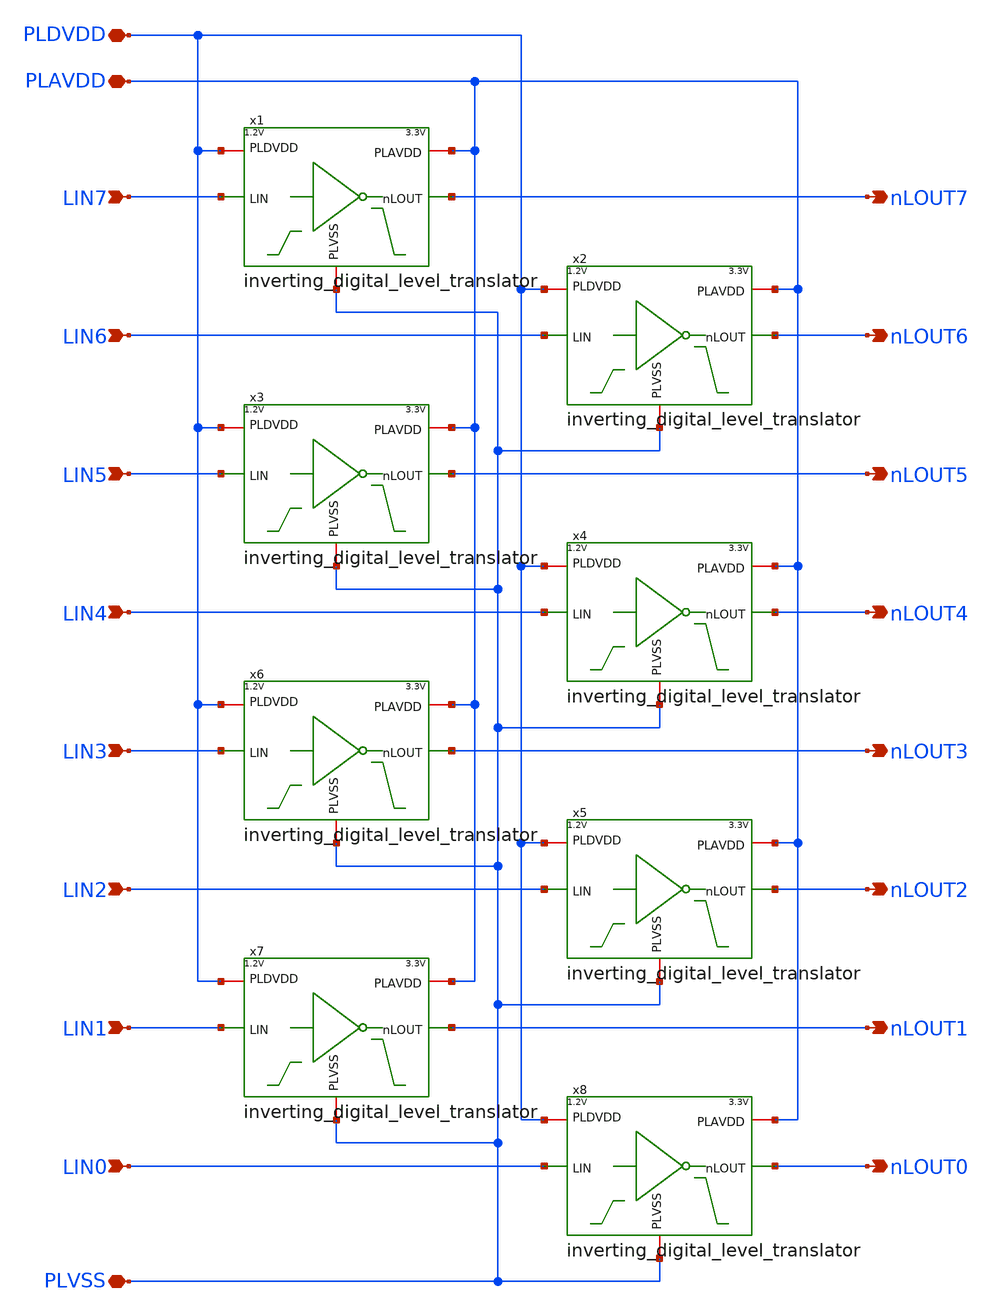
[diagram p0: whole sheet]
** sch_path: xschem/8x_inverting_digital_level_translator.sch
**.subckt 8x_inverting_digital_level_translator LIN7 nLOUT7 PLDVDD PLAVDD PLVSS LIN6 LIN5 LIN4 LIN3
*+ LIN2 LIN1 LIN0 nLOUT6 nLOUT5 nLOUT4 nLOUT3 nLOUT2 nLOUT1 nLOUT0
*.ipin LIN7
*.opin nLOUT7
*.iopin PLDVDD
*.iopin PLAVDD
*.iopin PLVSS
*.ipin LIN6
*.ipin LIN5
*.ipin LIN4
*.ipin LIN3
*.ipin LIN2
*.ipin LIN1
*.ipin LIN0
*.opin nLOUT6
*.opin nLOUT5
*.opin nLOUT4
*.opin nLOUT3
*.opin nLOUT2
*.opin nLOUT1
*.opin nLOUT0
x1 PLAVDD PLDVDD LIN7 nLOUT7 PLVSS inverting_digital_level_translator
x2 PLAVDD PLDVDD LIN6 nLOUT6 PLVSS inverting_digital_level_translator
x3 PLAVDD PLDVDD LIN5 nLOUT5 PLVSS inverting_digital_level_translator
x4 PLAVDD PLDVDD LIN4 nLOUT4 PLVSS inverting_digital_level_translator
x5 PLAVDD PLDVDD LIN2 nLOUT2 PLVSS inverting_digital_level_translator
x6 PLAVDD PLDVDD LIN3 nLOUT3 PLVSS inverting_digital_level_translator
x7 PLAVDD PLDVDD LIN1 nLOUT1 PLVSS inverting_digital_level_translator
x8 PLAVDD PLDVDD LIN0 nLOUT0 PLVSS inverting_digital_level_translator
**.ends

* expanding   symbol:  inverting_digital_level_translator.sym # of pins=5
** sym_path: xschem/inverting_digital_level_translator.sym
** sch_path: xschem/inverting_digital_level_translator.sch
.subckt inverting_digital_level_translator PLAVDD PLDVDD LIN nLOUT PLVSS
*.iopin PLAVDD
*.iopin PLVSS
*.iopin PLDVDD
*.ipin LIN
*.opin nLOUT
XM1 n_lin_buf net1 PLVSS PLVSS sg13_lv_nmos w=0.15u l=0.13u ng=1 m=1 mm_ok=1
XM2 n_lin_buf net1 PLDVDD PLDVDD sg13_lv_pmos w=0.3u l=0.13u ng=1 m=1 mm_ok=1
XM3 lin_buf n_lin_buf PLVSS PLVSS sg13_lv_nmos w=0.15u l=0.13u ng=1 m=1 mm_ok=1
XM4 lin_buf n_lin_buf PLDVDD PLDVDD sg13_lv_pmos w=0.3u l=0.13u ng=1 m=1 mm_ok=1
XM5 q_unbf n_lin_buf PLVSS PLVSS sg13_hv_nmos w=1u l=0.45u ng=1 m=1 mm_ok=1
XM6 n_q_unbf lin_buf PLVSS PLVSS sg13_hv_nmos w=1u l=0.45u ng=1 m=1 mm_ok=1
XM7 n_q_unbf q_unbf PLAVDD PLAVDD sg13_hv_pmos w=0.3u l=0.45u ng=1 m=1 mm_ok=1
XM9 nLOUT n_q_unbf PLVSS PLVSS sg13_hv_nmos w=0.3u l=0.45u ng=1 m=4 mm_ok=1
XM10 nLOUT n_q_unbf PLAVDD PLAVDD sg13_hv_pmos w=0.6u l=0.45u ng=1 m=4 mm_ok=1
XM8 q_unbf n_q_unbf PLAVDD PLAVDD sg13_hv_pmos w=0.3u l=0.45u ng=1 m=1 mm_ok=1
XM11 net1 LIN PLVSS PLVSS sg13_lv_nmos w=0.15u l=0.13u ng=1 m=1 mm_ok=1
XM12 net1 LIN PLDVDD PLDVDD sg13_lv_pmos w=0.3u l=0.13u ng=1 m=1 mm_ok=1
.ends

.end
